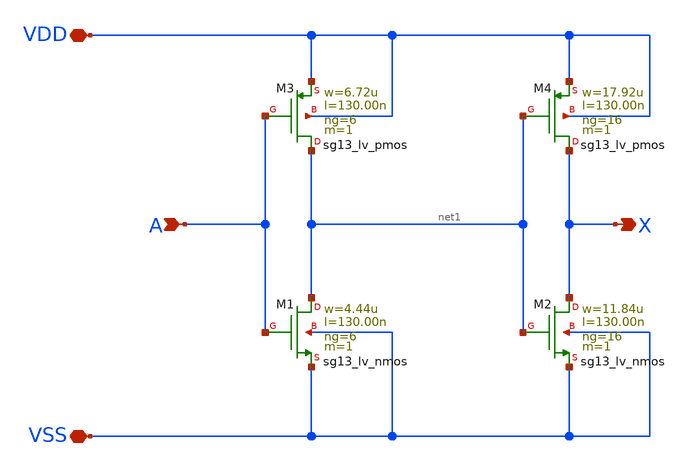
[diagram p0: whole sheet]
** sch_path: ihp-sg13g2/libs.tech/xschem/sg13g2_stdcells/sg13g2_buf_16.sch
* Copyright 2023 IHP PDK Authors
* Licensed under the Apache License, Version 2.0 (the "License");
* you may not use this file except in compliance with the License.
* You may obtain a copy of the License at
* https://www.apache.org/licenses/LICENSE-2.0
* Unless required by applicable law or agreed to in writing, software
* distributed under the License is distributed on an "AS IS" BASIS,
* WITHOUT WARRANTIES OR CONDITIONS OF ANY KIND, either express or implied.
* See the License for the specific language governing permissions and
* limitations under the License.
**.subckt sg13g2_buf_16 A X VDD VSS
*.ipin A
*.opin X
*.iopin VDD
*.iopin VSS
XM1 net1 A VSS VSS sg13_lv_nmos w=4.44u l=130.00n ng=6 m=1 mm_ok=1
XM2 X net1 VSS VSS sg13_lv_nmos w=11.84u l=130.00n ng=16 m=1 mm_ok=1
XM3 net1 A VDD VDD sg13_lv_pmos w=6.72u l=130.00n ng=6 m=1 mm_ok=1
XM4 X net1 VDD VDD sg13_lv_pmos w=17.92u l=130.00n ng=16 m=1 mm_ok=1
**.ends
.end
